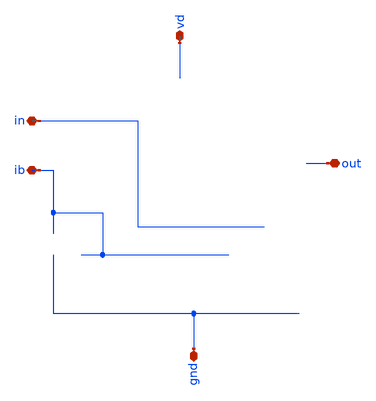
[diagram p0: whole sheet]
** sch_path: buffer/xschem/buffer-pex.sch
* Copyright 2020 Stefan Frederik Schippers
* Licensed under the Apache License, Version 2.0 (the "License");
* you may not use this file except in compliance with the License.
* You may obtain a copy of the License at
* https://www.apache.org/licenses/LICENSE-2.0
* Unless required by applicable law or agreed to in writing, software
* distributed under the License is distributed on an "AS IS" BASIS,
* WITHOUT WARRANTIES OR CONDITIONS OF ANY KIND, either express or implied.
* See the License for the specific language governing permissions and
* limitations under the License.
**.subckt buffer-pex vd ib out in gnd
*.iopin vd
*.iopin ib
*.iopin out
*.iopin in
*.iopin gnd
**** begin user architecture code


* NGSPICE file created from buffer.ext - technology: sky130A

*.subckt buffer vd ib out in gnd
X0 vd.t23 a d vd.t22 sky130_fd_pr__pfet_01v8 ad=0.145 pd=1.29 as=0.145 ps=1.29 w=1 l=1
X1 vd.t42 b.t10 out.t9 vd.t41 sky130_fd_pr__pfet_01v8 ad=0.29 pd=2.58 as=0.145 ps=1.29 w=1 l=1
X2 vd.t21 a d vd.t20 sky130_fd_pr__pfet_01v8 ad=0.145 pd=1.29 as=0.145 ps=1.29 w=1 l=1
X3 out.t8 b.t11 vd.t40 vd.t39 sky130_fd_pr__pfet_01v8 ad=0.145 pd=1.29 as=0.145 ps=1.29 w=1 l=1
X4 vd.t38 b.t12 out.t7 vd.t37 sky130_fd_pr__pfet_01v8 ad=0.145 pd=1.29 as=0.145 ps=1.29 w=1 l=1
X5 out.t6 b.t13 vd.t1 vd.t0 sky130_fd_pr__pfet_01v8 ad=0.145 pd=1.29 as=0.145 ps=1.29 w=1 l=1
X6 c.t9 in.t0 b.t2 gnd.t9 sky130_fd_pr__nfet_01v8 ad=0.145 pd=1.29 as=0.145 ps=1.29 w=1 l=1
X7 c.t8 in.t1 b.t6 gnd.t8 sky130_fd_pr__nfet_01v8 ad=0.145 pd=1.29 as=0.145 ps=1.29 w=1 l=1
X8 b.t8 in.t2 c.t7 gnd.t7 sky130_fd_pr__nfet_01v8 ad=0.145 pd=1.29 as=0.145 ps=1.29 w=1 l=1
X9 b.t5 in.t3 c.t6 gnd.t6 sky130_fd_pr__nfet_01v8 ad=0.145 pd=1.29 as=0.145 ps=1.29 w=1 l=1
X10 vd.t19 a d vd.t18 sky130_fd_pr__pfet_01v8 ad=0.145 pd=1.29 as=0.29 ps=2.58 w=1 l=1
X11 c.t20 out.t20 a gnd.t26 sky130_fd_pr__nfet_01v8 ad=0.145 pd=1.29 as=0.145 ps=1.29 w=1 l=1
X12 c.t19 out.t21 a gnd.t25 sky130_fd_pr__nfet_01v8 ad=0.145 pd=1.29 as=0.145 ps=1.29 w=1 l=1
X13 out.t10 d gnd.t61 gnd.t60 sky130_fd_pr__nfet_01v8 ad=0.145 pd=1.29 as=0.145 ps=1.29 w=1 l=1
X14 a a vd.t17 vd.t16 sky130_fd_pr__pfet_01v8 ad=0.29 pd=2.58 as=0.29 ps=2.58 w=1 l=1
X15 gnd.t67 d d gnd.t66 sky130_fd_pr__nfet_01v8 ad=0.145 pd=1.29 as=0.29 ps=2.58 w=1 l=1
X16 gnd.t65 d d gnd.t64 sky130_fd_pr__nfet_01v8 ad=0.145 pd=1.29 as=0.145 ps=1.29 w=1 l=1
X17 d a vd.t15 vd.t14 sky130_fd_pr__pfet_01v8 ad=0.29 pd=2.58 as=0.145 ps=1.29 w=1 l=1
X18 vd.t30 vd.t28 vd.t30 vd.t29 sky130_fd_pr__pfet_01v8 ad=0.145 pd=1.29 as=0 ps=0 w=1 l=1
X19 vd.t48 b.t14 out.t5 vd.t47 sky130_fd_pr__pfet_01v8 ad=0.145 pd=1.29 as=0.145 ps=1.29 w=1 l=1
X20 d a vd.t13 vd.t12 sky130_fd_pr__pfet_01v8 ad=0.145 pd=1.29 as=0.145 ps=1.29 w=1 l=1
X21 vd.t11 a d vd.t10 sky130_fd_pr__pfet_01v8 ad=0.145 pd=1.29 as=0.145 ps=1.29 w=1 l=1
X22 b.t0 in.t4 c.t5 gnd.t5 sky130_fd_pr__nfet_01v8 ad=0.145 pd=1.29 as=0.145 ps=1.29 w=1 l=1
X23 d d gnd.t63 gnd.t62 sky130_fd_pr__nfet_01v8 ad=0.145 pd=1.29 as=0.145 ps=1.29 w=1 l=1
X24 d d gnd.t59 gnd.t58 sky130_fd_pr__nfet_01v8 ad=0.145 pd=1.29 as=0.145 ps=1.29 w=1 l=1
X25 d a vd.t9 vd.t8 sky130_fd_pr__pfet_01v8 ad=0.145 pd=1.29 as=0.145 ps=1.29 w=1 l=1
X26 a out.t22 c.t18 gnd.t24 sky130_fd_pr__nfet_01v8 ad=0.145 pd=1.29 as=0.145 ps=1.29 w=1 l=1
X27 a out.t23 c.t17 gnd.t23 sky130_fd_pr__nfet_01v8 ad=0.145 pd=1.29 as=0.145 ps=1.29 w=1 l=1
X28 c.t16 out.t24 a gnd.t22 sky130_fd_pr__nfet_01v8 ad=0.145 pd=1.29 as=0.145 ps=1.29 w=1 l=1
X29 a out.t25 c.t15 gnd.t21 sky130_fd_pr__nfet_01v8 ad=0.145 pd=1.29 as=0.145 ps=1.29 w=1 l=1
X30 a a a gnd.t11 sky130_fd_pr__nfet_01v8 ad=0.145 pd=1.29 as=2.32 ps=20.6 w=1 l=1
X31 out.t11 d gnd.t57 gnd.t56 sky130_fd_pr__nfet_01v8 ad=0.145 pd=1.29 as=0.145 ps=1.29 w=1 l=1
X32 gnd.t55 d out.t12 gnd.t54 sky130_fd_pr__nfet_01v8 ad=0.145 pd=1.29 as=0.145 ps=1.29 w=1 l=1
X33 out.t13 d gnd.t53 gnd.t52 sky130_fd_pr__nfet_01v8 ad=0.145 pd=1.29 as=0.145 ps=1.29 w=1 l=1
X34 gnd.t51 d out.t14 gnd.t50 sky130_fd_pr__nfet_01v8 ad=0.145 pd=1.29 as=0.145 ps=1.29 w=1 l=1
X35 gnd.t49 d out.t15 gnd.t48 sky130_fd_pr__nfet_01v8 ad=0.145 pd=1.29 as=0.145 ps=1.29 w=1 l=1
X36 gnd.t47 d d gnd.t46 sky130_fd_pr__nfet_01v8 ad=0.145 pd=1.29 as=0.145 ps=1.29 w=1 l=1
X37 vd.t36 b.t15 out.t4 vd.t35 sky130_fd_pr__pfet_01v8 ad=0.145 pd=1.29 as=0.29 ps=2.58 w=1 l=1
X38 c.t4 in.t5 b.t7 gnd.t4 sky130_fd_pr__nfet_01v8 ad=0.145 pd=1.29 as=0.145 ps=1.29 w=1 l=1
X39 c.t3 in.t6 b.t9 gnd.t3 sky130_fd_pr__nfet_01v8 ad=0.145 pd=1.29 as=0.145 ps=1.29 w=1 l=1
X40 out.t26 d sky130_fd_pr__cap_mim_m3_2 l=15 w=30
X41 b.t4 in.t7 c.t2 gnd.t2 sky130_fd_pr__nfet_01v8 ad=0.145 pd=1.29 as=0.145 ps=1.29 w=1 l=1
X42 d d gnd.t45 gnd.t44 sky130_fd_pr__nfet_01v8 ad=0.145 pd=1.29 as=0.145 ps=1.29 w=1 l=1
X43 vd.t27 vd.t24 vd.t26 vd.t25 sky130_fd_pr__pfet_01v8 ad=0.29 pd=2.58 as=0 ps=0 w=1 l=1
X44 vd.t7 a d vd.t6 sky130_fd_pr__pfet_01v8 ad=0.29 pd=2.58 as=0.145 ps=1.29 w=1 l=1
X45 c.t14 out.t27 a gnd.t20 sky130_fd_pr__nfet_01v8 ad=0.145 pd=1.29 as=0.145 ps=1.29 w=1 l=1
X46 out.t16 d gnd.t43 gnd.t42 sky130_fd_pr__nfet_01v8 ad=0.145 pd=1.29 as=0.145 ps=1.29 w=1 l=1
X47 gnd.t41 d d gnd.t40 sky130_fd_pr__nfet_01v8 ad=0.145 pd=1.29 as=0.145 ps=1.29 w=1 l=1
X48 d d d gnd.t39 sky130_fd_pr__nfet_01v8 ad=0.145 pd=1.29 as=2.03 ps=18.1 w=1 l=1
X49 d a vd.t5 vd.t4 sky130_fd_pr__pfet_01v8 ad=0.145 pd=1.29 as=0.145 ps=1.29 w=1 l=1
X50 vd.t46 b.t16 out.t3 vd.t45 sky130_fd_pr__pfet_01v8 ad=0.145 pd=1.29 as=0.145 ps=1.29 w=1 l=1
X51 out.t2 b.t17 vd.t44 vd.t43 sky130_fd_pr__pfet_01v8 ad=0.145 pd=1.29 as=0.145 ps=1.29 w=1 l=1
X52 d a vd.t3 vd.t2 sky130_fd_pr__pfet_01v8 ad=0.145 pd=1.29 as=0.145 ps=1.29 w=1 l=1
X53 out.t1 b.t18 vd.t34 vd.t33 sky130_fd_pr__pfet_01v8 ad=0.145 pd=1.29 as=0.145 ps=1.29 w=1 l=1
X54 vd.t50 b.t19 out.t0 vd.t49 sky130_fd_pr__pfet_01v8 ad=0.145 pd=1.29 as=0.29 ps=2.58 w=1 l=1
X55 b b.t3 vd.t32 vd.t31 sky130_fd_pr__pfet_01v8 ad=0.29 pd=2.58 as=0.29 ps=2.58 w=1 l=1
X56 c.t1 in.t8 b.t1 gnd.t1 sky130_fd_pr__nfet_01v8 ad=0.145 pd=1.29 as=0.145 ps=1.29 w=1 l=1
X57 gnd.t13 ib.t3 ib.t4 gnd.t12 sky130_fd_pr__nfet_01v8 ad=0.145 pd=1.29 as=0.145 ps=1.29 w=1 l=1
X58 c.t10 ib.t5 gnd.t15 gnd.t14 sky130_fd_pr__nfet_01v8 ad=0.29 pd=2.58 as=0.145 ps=1.29 w=1 l=1
X59 b.t1 in.t9 c.t0 gnd.t0 sky130_fd_pr__nfet_01v8 ad=0.145 pd=1.29 as=0.145 ps=1.29 w=1 l=1
X60 ib.t2 ib.t0 ib.t1 gnd.t16 sky130_fd_pr__nfet_01v8 ad=0.29 pd=2.58 as=0 ps=0 w=1 l=1
X61 d d gnd.t38 gnd.t37 sky130_fd_pr__nfet_01v8 ad=0.145 pd=1.29 as=0.145 ps=1.29 w=1 l=1
X62 d d gnd.t36 gnd.t35 sky130_fd_pr__nfet_01v8 ad=0.145 pd=1.29 as=0.145 ps=1.29 w=1 l=1
X63 a a a gnd.t10 sky130_fd_pr__nfet_01v8 ad=0.29 pd=2.58 as=0 ps=0 w=1 l=1
X64 a out.t28 c.t13 gnd.t19 sky130_fd_pr__nfet_01v8 ad=0.145 pd=1.29 as=0.145 ps=1.29 w=1 l=1
X65 c.t12 out.t29 a gnd.t18 sky130_fd_pr__nfet_01v8 ad=0.145 pd=1.29 as=0.145 ps=1.29 w=1 l=1
X66 a out.t30 c.t11 gnd.t17 sky130_fd_pr__nfet_01v8 ad=0.145 pd=1.29 as=0.145 ps=1.29 w=1 l=1
X67 gnd.t34 d out.t17 gnd.t33 sky130_fd_pr__nfet_01v8 ad=0.145 pd=1.29 as=0.145 ps=1.29 w=1 l=1
X68 out.t18 d gnd.t32 gnd.t31 sky130_fd_pr__nfet_01v8 ad=0.145 pd=1.29 as=0.145 ps=1.29 w=1 l=1
X69 gnd.t30 d out.t19 gnd.t29 sky130_fd_pr__nfet_01v8 ad=0.145 pd=1.29 as=0.145 ps=1.29 w=1 l=1
X70 gnd.t28 d d gnd.t27 sky130_fd_pr__nfet_01v8 ad=0.145 pd=1.29 as=0.145 ps=1.29 w=1 l=1
R0 vd.n28 vd.n25 1304.47
R1 vd.n41 vd.n33 1070.68
R2 vd.t41 vd.t31 537.318
R3 vd.t31 vd.t49 526.24
R4 vd.t16 vd.t18 526.24
R5 vd.t14 vd.t16 512.391
R6 vd.t29 vd.t47 357.289
R7 vd.t47 vd.t0 357.289
R8 vd.t0 vd.t37 357.289
R9 vd.t49 vd.t39 357.289
R10 vd.t33 vd.t41 357.289
R11 vd.t45 vd.t33 357.289
R12 vd.t43 vd.t45 357.289
R13 vd.t6 vd.t12 357.289
R14 vd.t12 vd.t10 357.289
R15 vd.t10 vd.t8 357.289
R16 vd.t20 vd.t14 357.289
R17 vd.t4 vd.t20 357.289
R18 vd.t22 vd.t4 357.289
R19 vd.n24 vd.t29 354.529
R20 vd.n31 vd.t6 282.507
R21 vd.n31 vd.t35 254.811
R22 vd.n40 vd.n37 223.625
R23 vd.n34 vd.t2 204.957
R24 vd.n34 vd.t22 152.333
R25 vd.n26 vd.t43 144.024
R26 vd.n33 vd.n28 127.248
R27 vd.n41 vd.n40 117.835
R28 vd.n38 vd.t25 92.7848
R29 vd.n19 vd.t17 29.2512
R30 vd.n14 vd.t7 29.2303
R31 vd.n9 vd.t42 29.2303
R32 vd.n8 vd.t32 29.2303
R33 vd.n1 vd.t27 28.5795
R34 vd.n2 vd.t48 28.57
R35 vd.n0 vd.t3 28.5655
R36 vd.n0 vd.t26 28.5655
R37 vd.n22 vd.t5 28.5655
R38 vd.n22 vd.t23 28.5655
R39 vd.n20 vd.t15 28.5655
R40 vd.n20 vd.t21 28.5655
R41 vd.n17 vd.t9 28.5655
R42 vd.n17 vd.t19 28.5655
R43 vd.n15 vd.t13 28.5655
R44 vd.n15 vd.t11 28.5655
R45 vd.n12 vd.t44 28.5655
R46 vd.n12 vd.t36 28.5655
R47 vd.n10 vd.t34 28.5655
R48 vd.n10 vd.t46 28.5655
R49 vd.n6 vd.t40 28.5655
R50 vd.n6 vd.t50 28.5655
R51 vd.n4 vd.t1 28.5655
R52 vd.n4 vd.t38 28.5655
R53 vd.n1 vd.t24 19.8115
R54 vd.n3 vd.t28 19.8115
R55 vd.n2 vd.t30 14.2847
R56 vd.n5 vd.n3 1.47391
R57 vd vd.n1 1.0363
R58 vd.n8 vd.n7 1.0005
R59 vd.n19 vd.n18 1.0005
R60 vd.n7 vd.n5 0.813
R61 vd.n11 vd.n9 0.813
R62 vd.n18 vd.n16 0.813
R63 vd.n13 vd.n11 0.78175
R64 vd.n16 vd.n14 0.78175
R65 vd.n23 vd.n21 0.78175
R66 vd.n23 vd.n22 0.665316
R67 vd.n21 vd.n20 0.665316
R68 vd.n18 vd.n17 0.665316
R69 vd.n13 vd.n12 0.665316
R70 vd.n11 vd.n10 0.665316
R71 vd.n7 vd.n6 0.665316
R72 vd.n5 vd.n4 0.665316
R73 vd.n14 vd.n13 0.6255
R74 vd.n16 vd.n15 0.611443
R75 vd.n21 vd.n19 0.59425
R76 vd.n42 vd.n23 0.313
R77 vd.n9 vd.n8 0.21925
R78 vd vd.n42 0.0421667
R79 vd.n40 vd.n39 0.0168558
R80 vd.n39 vd.n38 0.0168558
R81 vd.n37 vd.n36 0.00979742
R82 vd.n25 vd.n24 0.00979742
R83 vd.n41 vd.n35 0.0055
R84 vd.n35 vd.n34 0.0055
R85 vd.n3 vd.n2 0.00500317
R86 vd.n1 vd.n0 0.00454578
R87 vd.n28 vd.n27 0.00186586
R88 vd.n27 vd.n26 0.00186586
R89 vd.n33 vd.n32 0.00173262
R90 vd.n32 vd.n31 0.00173262
R91 vd.n30 vd.n29 0.00111631
R92 vd.n31 vd.n30 0.00111631
R93 vd.n42 vd.n41 0.000511142
R94 b.n0 b.t15 40.2461
R95 b.n2 b.t14 40.2461
R96 b b.t3 39.5317
R97 b.n1 b.t10 39.5292
R98 b.n1 b.t18 39.5292
R99 b.n0 b.t16 39.5292
R100 b.n0 b.t17 39.5292
R101 b.n3 b.t19 39.5292
R102 b.n3 b.t11 39.5292
R103 b.n2 b.t12 39.5292
R104 b.n2 b.t13 39.5292
R105 b.n5 b.t6 17.4005
R106 b.n5 b.t5 17.4005
R107 b.n6 b.t7 17.4005
R108 b.n6 b.t4 17.4005
R109 b.n7 b.t2 17.4005
R110 b.n7 b.t8 17.4005
R111 b.n4 b.t9 17.4005
R112 b.n4 b.t0 17.4005
R113 b.n4 b.n5 3.17253
R114 b.n6 b.n7 2.69321
R115 b.n5 b.n6 2.68836
R116 b.t1 b.n4 2.65092
R117 b.n3 b.n2 2.15117
R118 b.n1 b.n0 2.15117
R119 b b.n1 1.49152
R120 b b.t1 0.968485
R121 b b.n3 0.961845
R122 out.n7 out.t4 30.2161
R123 out.n4 out.t0 29.2293
R124 out.n5 out.t9 28.5655
R125 out.n5 out.t1 28.5655
R126 out.n6 out.t3 28.5655
R127 out.n6 out.t2 28.5655
R128 out.n2 out.t7 28.5655
R129 out.n2 out.t8 28.5655
R130 out.n1 out.t5 28.5655
R131 out.n1 out.t6 28.5655
R132 out.n20 out.t20 26.8319
R133 out.n21 out.t27 25.9449
R134 out.n26 out.t30 25.7428
R135 out.n27 out.t21 25.5407
R136 out.n22 out.t28 25.3386
R137 out.n23 out.t29 25.1365
R138 out.n20 out.t22 24.9306
R139 out.n28 out.t25 24.696
R140 out.n25 out.t24 24.5271
R141 out.n24 out.t23 24.1037
R142 out.n0 out.t15 17.4005
R143 out.n0 out.t10 17.4005
R144 out.n10 out.t19 17.4005
R145 out.n10 out.t18 17.4005
R146 out.n11 out.t14 17.4005
R147 out.n11 out.t13 17.4005
R148 out.n12 out.t17 17.4005
R149 out.n12 out.t16 17.4005
R150 out.n13 out.t12 17.4005
R151 out.n13 out.t11 17.4005
R152 out.n14 out.n13 2.74907
R153 out.n17 out.n9 2.41728
R154 out.n24 out.n23 2.30343
R155 out.n22 out.n21 2.29903
R156 out.n28 out.n27 2.2903
R157 out.n26 out.n25 2.25283
R158 out.n16 out.n15 2.1255
R159 out.n15 out.n14 2.1255
R160 out.n29 out.n19 1.97968
R161 out.n18 out.n17 1.83383
R162 out.n3 out.n1 1.74765
R163 out.n19 out.t26 1.69869
R164 out out.n29 1.60362
R165 out.n29 out.n28 1.24394
R166 out.n8 out.n7 1.04217
R167 out.n4 out.n3 1.0005
R168 out.n9 out.n4 0.938
R169 out.n25 out.n24 0.680308
R170 out.n23 out.n22 0.678839
R171 out.n27 out.n26 0.678839
R172 out.n8 out.n5 0.664316
R173 out.n3 out.n2 0.664316
R174 out.n9 out.n8 0.646333
R175 out.n21 out.n20 0.63023
R176 out.n7 out.n6 0.610444
R177 out.n18 out.n0 0.582399
R178 out.n15 out.n11 0.582399
R179 out.n14 out.n12 0.582399
R180 out.n16 out.n10 0.579923
R181 out.n17 out.n16 0.333833
R182 out.n19 out.n18 0.250559
R183 in.n1 in.t6 27.6073
R184 in.n6 in.t7 27.1628
R185 in.n5 in.t5 26.7019
R186 in.n0 in.t8 26.4053
R187 in.n0 in.t9 26.2229
R188 in.n4 in.t3 25.2012
R189 in.n2 in.t4 25.2012
R190 in.n7 in.t0 24.699
R191 in.n3 in.t1 24.699
R192 in.n8 in.t2 24.1526
R193 in in.n8 2.98635
R194 in.n5 in.n4 2.30564
R195 in.n1 in.n0 2.30482
R196 in.n3 in.n2 2.27981
R197 in.n7 in.n6 2.24388
R198 in.n6 in.n5 0.680761
R199 in.n4 in.n3 0.680308
R200 in.n8 in.n7 0.680308
R201 in.n2 in.n1 0.604164
R202 c c.t10 18.4486
R203 c.n17 c.t7 17.4005
R204 c.n17 c.t20 17.4005
R205 c.n13 c.t2 17.4005
R206 c.n13 c.t14 17.4005
R207 c.n11 c.t13 17.4005
R208 c.n11 c.t4 17.4005
R209 c.n9 c.t6 17.4005
R210 c.n9 c.t12 17.4005
R211 c.n7 c.t17 17.4005
R212 c.n7 c.t8 17.4005
R213 c.n5 c.t5 17.4005
R214 c.n5 c.t16 17.4005
R215 c.n3 c.t11 17.4005
R216 c.n3 c.t3 17.4005
R217 c.n1 c.t0 17.4005
R218 c.n1 c.t19 17.4005
R219 c.n0 c.t15 17.4005
R220 c.n0 c.t1 17.4005
R221 c.n15 c.t18 17.4005
R222 c.n15 c.t9 17.4005
R223 c.n2 c.n0 1.87829
R224 c c.n18 1.52139
R225 c.n18 c.n17 1.51465
R226 c.n4 c.n2 1.08383
R227 c.n6 c.n4 1.08383
R228 c.n10 c.n8 1.08383
R229 c.n12 c.n10 1.08383
R230 c.n14 c.n12 1.08383
R231 c.n8 c.n6 1.04217
R232 c.n16 c.n14 1.04217
R233 c.n6 c.n5 0.776026
R234 c.n14 c.n13 0.766495
R235 c.n4 c.n3 0.766495
R236 c.n12 c.n11 0.766495
R237 c.n10 c.n9 0.766495
R238 c.n8 c.n7 0.766495
R239 c.n2 c.n1 0.766495
R240 c.n16 c.n15 0.766495
R241 c.n18 c.n16 0.333833
R242 gnd.n30 gnd.n29 1273.6
R243 gnd.n26 gnd.n23 1260.8
R244 gnd.n51 gnd.n39 1088.88
R245 gnd.t58 gnd.t48 202.462
R246 gnd.t21 gnd.t60 188.337
R247 gnd.t1 gnd.t64 188.337
R248 gnd.t0 gnd.t35 188.337
R249 gnd.t25 gnd.t29 188.337
R250 gnd.t17 gnd.t31 188.337
R251 gnd.t3 gnd.t40 188.337
R252 gnd.t5 gnd.t62 188.337
R253 gnd.t37 gnd.t6 188.337
R254 gnd.t19 gnd.t42 188.337
R255 gnd.t4 gnd.t27 188.337
R256 gnd.t2 gnd.t44 188.337
R257 gnd.t20 gnd.t54 188.337
R258 gnd.t24 gnd.t56 188.337
R259 gnd.t9 gnd.t66 188.337
R260 gnd.n24 gnd.t50 131.835
R261 gnd.t46 gnd.n34 130.267
R262 gnd.t14 gnd.t9 128.696
R263 gnd.t12 gnd.t7 128.696
R264 gnd.n37 gnd.t52 113.002
R265 gnd.n48 gnd.n47 112.218
R266 gnd.n27 gnd.t58 109.079
R267 gnd.n40 gnd.t16 103.585
R268 gnd.n27 gnd.t39 93.3838
R269 gnd.n39 gnd.n26 88.0946
R270 gnd.n37 gnd.t23 75.3349
R271 gnd.t7 gnd.t14 73.7654
R272 gnd.t26 gnd.t12 73.7654
R273 gnd.n47 gnd.n44 62.7792
R274 gnd.n51 gnd.n50 60.3613
R275 gnd.n34 gnd.t8 58.0708
R276 gnd.n40 gnd.t26 25.112
R277 gnd.n19 gnd.t15 17.4005
R278 gnd.n19 gnd.t13 17.4005
R279 gnd.n17 gnd.t57 17.4005
R280 gnd.n17 gnd.t67 17.4005
R281 gnd.n15 gnd.t45 17.4005
R282 gnd.n15 gnd.t55 17.4005
R283 gnd.n13 gnd.t43 17.4005
R284 gnd.n13 gnd.t28 17.4005
R285 gnd.n11 gnd.t38 17.4005
R286 gnd.n11 gnd.t34 17.4005
R287 gnd.n9 gnd.t53 17.4005
R288 gnd.n9 gnd.t47 17.4005
R289 gnd.n7 gnd.t63 17.4005
R290 gnd.n7 gnd.t51 17.4005
R291 gnd.n5 gnd.t32 17.4005
R292 gnd.n5 gnd.t41 17.4005
R293 gnd.n3 gnd.t36 17.4005
R294 gnd.n3 gnd.t30 17.4005
R295 gnd.n1 gnd.t61 17.4005
R296 gnd.n1 gnd.t65 17.4005
R297 gnd.n0 gnd.t59 17.4005
R298 gnd.n0 gnd.t49 17.4005
R299 gnd.t60 gnd.t11 14.1257
R300 gnd.t64 gnd.t21 14.1257
R301 gnd.t35 gnd.t1 14.1257
R302 gnd.t29 gnd.t0 14.1257
R303 gnd.t31 gnd.t25 14.1257
R304 gnd.t40 gnd.t17 14.1257
R305 gnd.t62 gnd.t3 14.1257
R306 gnd.t50 gnd.t5 14.1257
R307 gnd.t52 gnd.t22 14.1257
R308 gnd.t23 gnd.t46 14.1257
R309 gnd.t8 gnd.t37 14.1257
R310 gnd.t6 gnd.t33 14.1257
R311 gnd.t42 gnd.t18 14.1257
R312 gnd.t27 gnd.t19 14.1257
R313 gnd.t44 gnd.t4 14.1257
R314 gnd.t54 gnd.t2 14.1257
R315 gnd.t56 gnd.t20 14.1257
R316 gnd.t66 gnd.t24 14.1257
R317 gnd.n48 gnd.t10 6.27837
R318 gnd.n2 gnd.n0 1.66573
R319 gnd.n20 gnd.n18 1.3755
R320 gnd.n4 gnd.n2 1.08383
R321 gnd.n8 gnd.n6 1.08383
R322 gnd.n10 gnd.n8 1.08383
R323 gnd.n12 gnd.n10 1.08383
R324 gnd.n16 gnd.n14 1.08383
R325 gnd.n18 gnd.n16 1.08383
R326 gnd.n6 gnd.n4 1.04217
R327 gnd.n14 gnd.n12 1.04217
R328 gnd.n18 gnd.n17 0.582399
R329 gnd.n16 gnd.n15 0.582399
R330 gnd.n14 gnd.n13 0.582399
R331 gnd.n12 gnd.n11 0.582399
R332 gnd.n10 gnd.n9 0.582399
R333 gnd.n8 gnd.n7 0.582399
R334 gnd.n6 gnd.n5 0.582399
R335 gnd.n2 gnd.n1 0.582399
R336 gnd.n4 gnd.n3 0.579923
R337 gnd.n20 gnd.n19 0.57713
R338 gnd.n52 gnd.n20 0.392443
R339 gnd.n50 gnd.n49 0.288252
R340 gnd.n49 gnd.n48 0.288252
R341 gnd.n53 gnd.n52 0.101164
R342 gnd.n53 gnd 0.093
R343 gnd gnd.n53 0.0823584
R344 gnd.n43 gnd.n42 0.0425017
R345 gnd.n44 gnd.n43 0.0425017
R346 gnd.n29 gnd.n28 0.0425017
R347 gnd.n28 gnd.n27 0.0425017
R348 gnd.n46 gnd.n45 0.0425017
R349 gnd.n47 gnd.n46 0.0425017
R350 gnd.n23 gnd.n22 0.0425017
R351 gnd.n22 gnd.n21 0.0425017
R352 gnd.n26 gnd.n25 0.00498892
R353 gnd.n25 gnd.n24 0.00498892
R354 gnd.n39 gnd.n38 0.00466542
R355 gnd.n38 gnd.n37 0.00466542
R356 gnd.n31 gnd.n30 0.00271942
R357 gnd.n34 gnd.n31 0.00271942
R358 gnd.n33 gnd.n32 0.00271942
R359 gnd.n34 gnd.n33 0.00271942
R360 gnd.n36 gnd.n35 0.00258271
R361 gnd.n37 gnd.n36 0.00258271
R362 gnd.n51 gnd.n41 0.00190526
R363 gnd.n41 gnd.n40 0.00190526
R364 gnd.n52 gnd.n51 0.000503131
R365 ib.n1 ib.t5 38.0465
R366 ib.n1 ib.t3 37.3602
R367 ib.n3 ib.t0 18.7313
R368 ib.n3 ib.t2 17.409
R369 ib.n0 ib.t4 17.4005
R370 ib.n0 ib.t1 17.4005
R371 ib ib.n4 1.26488
R372 ib.n2 ib.n1 0.239515
R373 ib.n4 ib.n3 0.0163842
R374 ib.n2 ib.n0 0.00444823
R375 ib.n4 ib.n2 0.00358796
C0 in ib 0.0558f
C1 d ib 0.12f
C2 b ib 0.0167f
C3 ib out 0.0112f
C4 ib a 0.0692f
C5 vd c 0.0419f
C6 in vd 0.145f
C7 vd d 1.97f
C8 in c 1.08f
C9 d c 1.32f
C10 b vd 5.7f
C11 vd a 5.74f
C12 vd out 2.13f
C13 in d 0.207f
C14 b c 1.34f
C15 out c 2.02f
C16 c a 3.88f
C17 b in 2.94f
C18 b d 1.04f
C19 in a 0.643f
C20 in out 2.36f
C21 d a 2.4f
C22 d out 40f
C23 vd ib 4.52e-19
C24 b a 0.126f
C25 b out 2.8f
C26 ib c 0.0951f
C27 out a 3.96f
*.ends



**** end user architecture code
**.ends
.end
